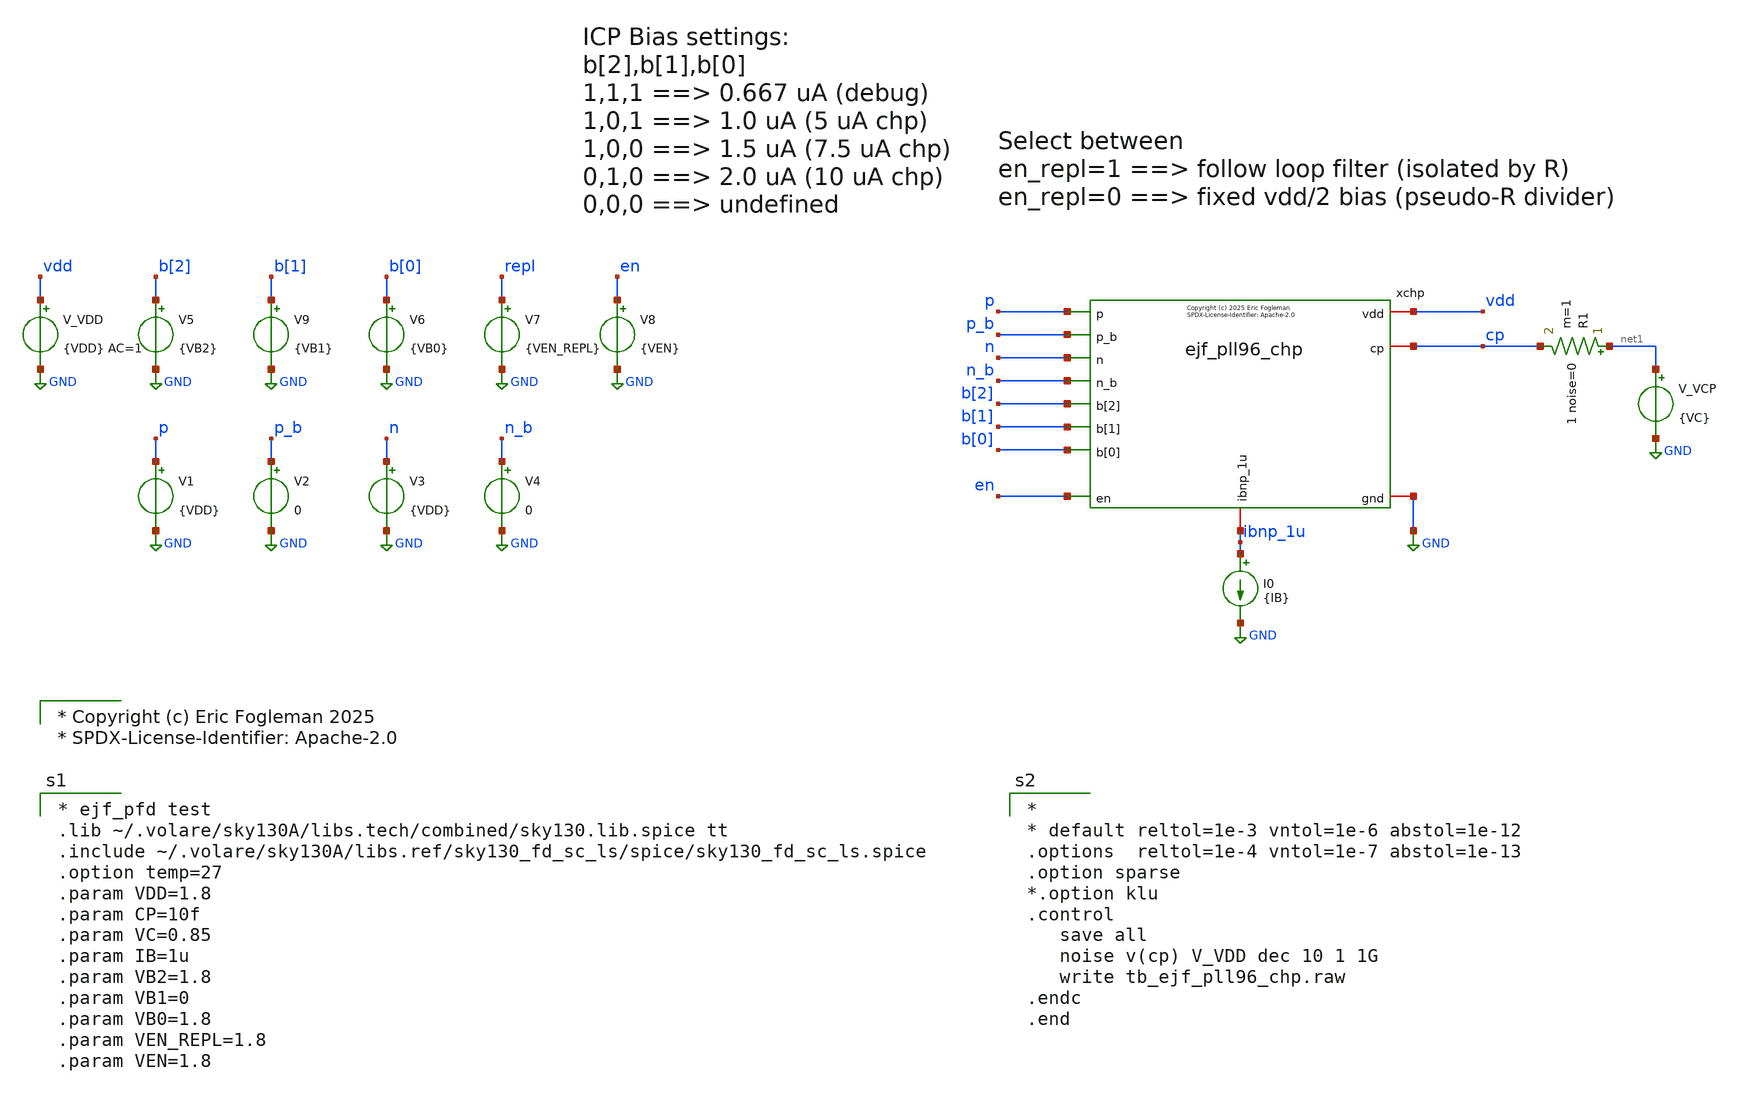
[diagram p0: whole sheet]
** sch_path: xschem/tb_ejf_pll96_chp.sch
* xschem/ejf_pll96_chp.sym:
* Copyright (c) 2025 Eric Fogleman

* Copyright (c) Eric Fogleman 2025
* SPDX-License-Identifier: Apache-2.0

**.subckt tb_ejf_pll96_chp
V_VDD vdd GND {VDD} AC=1
.save i(v_vdd)
xchp vdd p ibnp_1u p_b cp n_b n GND b[1] en b[2] b[0] ejf_pll96_chp
I0 ibnp_1u GND {IB}
V_VCP net1 GND {VC}
.save i(v_vcp)
V1 p GND {VDD}
.save i(v1)
V2 p_b GND 0
.save i(v2)
V3 n GND {VDD}
.save i(v3)
V4 n_b GND 0
.save i(v4)
R1 net1 cp 1 noise=0 m=1
V5 b[2] GND {VB2}
.save i(v5)
V6 b[0] GND {VB0}
.save i(v6)
V7 repl GND {VEN_REPL}
.save i(v7)
V8 en GND {VEN}
.save i(v8)
V9 b[1] GND {VB1}
.save i(v9)
**** begin user architecture code

* ejf_pfd test
.lib ~/.volare/sky130A/libs.tech/combined/sky130.lib.spice tt
.include ~/.volare/sky130A/libs.ref/sky130_fd_sc_ls/spice/sky130_fd_sc_ls.spice
.option temp=27
.param VDD=1.8
.param CP=10f
.param VC=0.85
.param IB=1u
.param VB2=1.8
.param VB1=0
.param VB0=1.8
.param VEN_REPL=1.8
.param VEN=1.8



*
* default reltol=1e-3 vntol=1e-6 abstol=1e-12
.options  reltol=1e-4 vntol=1e-7 abstol=1e-13
.option sparse
*.option klu
.control
   save all
   noise v(cp) V_VDD dec 10 1 1G
   write tb_ejf_pll96_chp.raw
.endc
.end

**** end user architecture code
**.ends

* expanding   symbol:  ejf_pll96_chp.sym # of pins=12
** sym_path: xschem/ejf_pll96_chp.sym
** sch_path: xschem/ejf_pll96_chp.sch
.subckt ejf_pll96_chp vdd p ibnp_1u p_b cp n_b n gnd b[1] en b[2] b[0]
*.iopin vdd
*.iopin gnd
*.iopin ibnp_1u
*.iopin cp
*.ipin p
*.ipin n_b
*.ipin p_b
*.ipin n
*.ipin en
*.ipin b[2]
*.ipin b[1]
*.ipin b[0]
XMP2_2[1] mp2d mp2_2g vdd vdd sky130_fd_pr__pfet_01v8_lvt L=1.2 W=0.6 nf=1 ad='int((nf+1)/2) * W/nf * 0.29'
+ as='int((nf+2)/2) * W/nf * 0.29' pd='2*int((nf+1)/2) * (W/nf + 0.29)' ps='2*int((nf+2)/2) * (W/nf + 0.29)'
+ nrd='0.29 / W' nrs='0.29 / W' sa=0 sb=0 sd=0 mult=1 m=1
XMP2_2[0] mp2d mp2_2g vdd vdd sky130_fd_pr__pfet_01v8_lvt L=1.2 W=0.6 nf=1 ad='int((nf+1)/2) * W/nf * 0.29'
+ as='int((nf+2)/2) * W/nf * 0.29' pd='2*int((nf+1)/2) * (W/nf + 0.29)' ps='2*int((nf+2)/2) * (W/nf + 0.29)'
+ nrd='0.29 / W' nrs='0.29 / W' sa=0 sb=0 sd=0 mult=1 m=1
XMN3 net1 mn1g gnd gnd sky130_fd_pr__nfet_01v8 L=1.2 W=0.6 nf=1 ad='int((nf+1)/2) * W/nf * 0.29' as='int((nf+2)/2) * W/nf * 0.29'
+ pd='2*int((nf+1)/2) * (W/nf + 0.29)' ps='2*int((nf+2)/2) * (W/nf + 0.29)' nrd='0.29 / W' nrs='0.29 / W'
+ sa=0 sb=0 sd=0 mult=1 m=1
XMN3C mn1g mn1cg net1 gnd sky130_fd_pr__nfet_01v8 L=0.3 W=0.6 nf=1 ad='int((nf+1)/2) * W/nf * 0.29' as='int((nf+2)/2) * W/nf * 0.29'
+ pd='2*int((nf+1)/2) * (W/nf + 0.29)' ps='2*int((nf+2)/2) * (W/nf + 0.29)' nrd='0.29 / W' nrs='0.29 / W'
+ sa=0 sb=0 sd=0 mult=1 m=1
XMP1[14] mp1d mp1g vdd vdd sky130_fd_pr__pfet_01v8_lvt L=1.2 W=0.6 nf=1 ad='int((nf+1)/2) * W/nf * 0.29'
+ as='int((nf+2)/2) * W/nf * 0.29' pd='2*int((nf+1)/2) * (W/nf + 0.29)' ps='2*int((nf+2)/2) * (W/nf + 0.29)'
+ nrd='0.29 / W' nrs='0.29 / W' sa=0 sb=0 sd=0 mult=1 m=1
XMP1[13] mp1d mp1g vdd vdd sky130_fd_pr__pfet_01v8_lvt L=1.2 W=0.6 nf=1 ad='int((nf+1)/2) * W/nf * 0.29'
+ as='int((nf+2)/2) * W/nf * 0.29' pd='2*int((nf+1)/2) * (W/nf + 0.29)' ps='2*int((nf+2)/2) * (W/nf + 0.29)'
+ nrd='0.29 / W' nrs='0.29 / W' sa=0 sb=0 sd=0 mult=1 m=1
XMP1[12] mp1d mp1g vdd vdd sky130_fd_pr__pfet_01v8_lvt L=1.2 W=0.6 nf=1 ad='int((nf+1)/2) * W/nf * 0.29'
+ as='int((nf+2)/2) * W/nf * 0.29' pd='2*int((nf+1)/2) * (W/nf + 0.29)' ps='2*int((nf+2)/2) * (W/nf + 0.29)'
+ nrd='0.29 / W' nrs='0.29 / W' sa=0 sb=0 sd=0 mult=1 m=1
XMP1[11] mp1d mp1g vdd vdd sky130_fd_pr__pfet_01v8_lvt L=1.2 W=0.6 nf=1 ad='int((nf+1)/2) * W/nf * 0.29'
+ as='int((nf+2)/2) * W/nf * 0.29' pd='2*int((nf+1)/2) * (W/nf + 0.29)' ps='2*int((nf+2)/2) * (W/nf + 0.29)'
+ nrd='0.29 / W' nrs='0.29 / W' sa=0 sb=0 sd=0 mult=1 m=1
XMP1[10] mp1d mp1g vdd vdd sky130_fd_pr__pfet_01v8_lvt L=1.2 W=0.6 nf=1 ad='int((nf+1)/2) * W/nf * 0.29'
+ as='int((nf+2)/2) * W/nf * 0.29' pd='2*int((nf+1)/2) * (W/nf + 0.29)' ps='2*int((nf+2)/2) * (W/nf + 0.29)'
+ nrd='0.29 / W' nrs='0.29 / W' sa=0 sb=0 sd=0 mult=1 m=1
XMP1[9] mp1d mp1g vdd vdd sky130_fd_pr__pfet_01v8_lvt L=1.2 W=0.6 nf=1 ad='int((nf+1)/2) * W/nf * 0.29'
+ as='int((nf+2)/2) * W/nf * 0.29' pd='2*int((nf+1)/2) * (W/nf + 0.29)' ps='2*int((nf+2)/2) * (W/nf + 0.29)'
+ nrd='0.29 / W' nrs='0.29 / W' sa=0 sb=0 sd=0 mult=1 m=1
XMP1[8] mp1d mp1g vdd vdd sky130_fd_pr__pfet_01v8_lvt L=1.2 W=0.6 nf=1 ad='int((nf+1)/2) * W/nf * 0.29'
+ as='int((nf+2)/2) * W/nf * 0.29' pd='2*int((nf+1)/2) * (W/nf + 0.29)' ps='2*int((nf+2)/2) * (W/nf + 0.29)'
+ nrd='0.29 / W' nrs='0.29 / W' sa=0 sb=0 sd=0 mult=1 m=1
XMP1[7] mp1d mp1g vdd vdd sky130_fd_pr__pfet_01v8_lvt L=1.2 W=0.6 nf=1 ad='int((nf+1)/2) * W/nf * 0.29'
+ as='int((nf+2)/2) * W/nf * 0.29' pd='2*int((nf+1)/2) * (W/nf + 0.29)' ps='2*int((nf+2)/2) * (W/nf + 0.29)'
+ nrd='0.29 / W' nrs='0.29 / W' sa=0 sb=0 sd=0 mult=1 m=1
XMP1[6] mp1d mp1g vdd vdd sky130_fd_pr__pfet_01v8_lvt L=1.2 W=0.6 nf=1 ad='int((nf+1)/2) * W/nf * 0.29'
+ as='int((nf+2)/2) * W/nf * 0.29' pd='2*int((nf+1)/2) * (W/nf + 0.29)' ps='2*int((nf+2)/2) * (W/nf + 0.29)'
+ nrd='0.29 / W' nrs='0.29 / W' sa=0 sb=0 sd=0 mult=1 m=1
XMP1[5] mp1d mp1g vdd vdd sky130_fd_pr__pfet_01v8_lvt L=1.2 W=0.6 nf=1 ad='int((nf+1)/2) * W/nf * 0.29'
+ as='int((nf+2)/2) * W/nf * 0.29' pd='2*int((nf+1)/2) * (W/nf + 0.29)' ps='2*int((nf+2)/2) * (W/nf + 0.29)'
+ nrd='0.29 / W' nrs='0.29 / W' sa=0 sb=0 sd=0 mult=1 m=1
XMP1[4] mp1d mp1g vdd vdd sky130_fd_pr__pfet_01v8_lvt L=1.2 W=0.6 nf=1 ad='int((nf+1)/2) * W/nf * 0.29'
+ as='int((nf+2)/2) * W/nf * 0.29' pd='2*int((nf+1)/2) * (W/nf + 0.29)' ps='2*int((nf+2)/2) * (W/nf + 0.29)'
+ nrd='0.29 / W' nrs='0.29 / W' sa=0 sb=0 sd=0 mult=1 m=1
XMP1[3] mp1d mp1g vdd vdd sky130_fd_pr__pfet_01v8_lvt L=1.2 W=0.6 nf=1 ad='int((nf+1)/2) * W/nf * 0.29'
+ as='int((nf+2)/2) * W/nf * 0.29' pd='2*int((nf+1)/2) * (W/nf + 0.29)' ps='2*int((nf+2)/2) * (W/nf + 0.29)'
+ nrd='0.29 / W' nrs='0.29 / W' sa=0 sb=0 sd=0 mult=1 m=1
XMP1[2] mp1d mp1g vdd vdd sky130_fd_pr__pfet_01v8_lvt L=1.2 W=0.6 nf=1 ad='int((nf+1)/2) * W/nf * 0.29'
+ as='int((nf+2)/2) * W/nf * 0.29' pd='2*int((nf+1)/2) * (W/nf + 0.29)' ps='2*int((nf+2)/2) * (W/nf + 0.29)'
+ nrd='0.29 / W' nrs='0.29 / W' sa=0 sb=0 sd=0 mult=1 m=1
XMP1[1] mp1d mp1g vdd vdd sky130_fd_pr__pfet_01v8_lvt L=1.2 W=0.6 nf=1 ad='int((nf+1)/2) * W/nf * 0.29'
+ as='int((nf+2)/2) * W/nf * 0.29' pd='2*int((nf+1)/2) * (W/nf + 0.29)' ps='2*int((nf+2)/2) * (W/nf + 0.29)'
+ nrd='0.29 / W' nrs='0.29 / W' sa=0 sb=0 sd=0 mult=1 m=1
XMP1[0] mp1d mp1g vdd vdd sky130_fd_pr__pfet_01v8_lvt L=1.2 W=0.6 nf=1 ad='int((nf+1)/2) * W/nf * 0.29'
+ as='int((nf+2)/2) * W/nf * 0.29' pd='2*int((nf+1)/2) * (W/nf + 0.29)' ps='2*int((nf+2)/2) * (W/nf + 0.29)'
+ nrd='0.29 / W' nrs='0.29 / W' sa=0 sb=0 sd=0 mult=1 m=1
XMP2C mp1g ibnp_1u mp2d vdd sky130_fd_pr__pfet_01v8_lvt L=0.35 W=1.2 nf=1 ad='int((nf+1)/2) * W/nf * 0.29'
+ as='int((nf+2)/2) * W/nf * 0.29' pd='2*int((nf+1)/2) * (W/nf + 0.29)' ps='2*int((nf+2)/2) * (W/nf + 0.29)'
+ nrd='0.29 / W' nrs='0.29 / W' sa=0 sb=0 sd=0 mult=1 m=1
XMP1C mp1cd ibnp_1u mp1d vdd sky130_fd_pr__pfet_01v8_lvt L=0.35 W=6 nf=5 ad='int((nf+1)/2) * W/nf * 0.29'
+ as='int((nf+2)/2) * W/nf * 0.29' pd='2*int((nf+1)/2) * (W/nf + 0.29)' ps='2*int((nf+2)/2) * (W/nf + 0.29)'
+ nrd='0.29 / W' nrs='0.29 / W' sa=0 sb=0 sd=0 mult=1 m=1
XMN1[4] mn1d mn1g gnd gnd sky130_fd_pr__nfet_01v8 L=1.2 W=0.6 nf=1 ad='int((nf+1)/2) * W/nf * 0.29' as='int((nf+2)/2) * W/nf * 0.29'
+ pd='2*int((nf+1)/2) * (W/nf + 0.29)' ps='2*int((nf+2)/2) * (W/nf + 0.29)' nrd='0.29 / W' nrs='0.29 / W'
+ sa=0 sb=0 sd=0 mult=1 m=1
XMN1[3] mn1d mn1g gnd gnd sky130_fd_pr__nfet_01v8 L=1.2 W=0.6 nf=1 ad='int((nf+1)/2) * W/nf * 0.29' as='int((nf+2)/2) * W/nf * 0.29'
+ pd='2*int((nf+1)/2) * (W/nf + 0.29)' ps='2*int((nf+2)/2) * (W/nf + 0.29)' nrd='0.29 / W' nrs='0.29 / W'
+ sa=0 sb=0 sd=0 mult=1 m=1
XMN1[2] mn1d mn1g gnd gnd sky130_fd_pr__nfet_01v8 L=1.2 W=0.6 nf=1 ad='int((nf+1)/2) * W/nf * 0.29' as='int((nf+2)/2) * W/nf * 0.29'
+ pd='2*int((nf+1)/2) * (W/nf + 0.29)' ps='2*int((nf+2)/2) * (W/nf + 0.29)' nrd='0.29 / W' nrs='0.29 / W'
+ sa=0 sb=0 sd=0 mult=1 m=1
XMN1[1] mn1d mn1g gnd gnd sky130_fd_pr__nfet_01v8 L=1.2 W=0.6 nf=1 ad='int((nf+1)/2) * W/nf * 0.29' as='int((nf+2)/2) * W/nf * 0.29'
+ pd='2*int((nf+1)/2) * (W/nf + 0.29)' ps='2*int((nf+2)/2) * (W/nf + 0.29)' nrd='0.29 / W' nrs='0.29 / W'
+ sa=0 sb=0 sd=0 mult=1 m=1
XMN1[0] mn1d mn1g gnd gnd sky130_fd_pr__nfet_01v8 L=1.2 W=0.6 nf=1 ad='int((nf+1)/2) * W/nf * 0.29' as='int((nf+2)/2) * W/nf * 0.29'
+ pd='2*int((nf+1)/2) * (W/nf + 0.29)' ps='2*int((nf+2)/2) * (W/nf + 0.29)' nrd='0.29 / W' nrs='0.29 / W'
+ sa=0 sb=0 sd=0 mult=1 m=1
XM1C mn1cd mn1cg mn1d gnd sky130_fd_pr__nfet_01v8 L=0.3 W=3.0 nf=5 ad='int((nf+1)/2) * W/nf * 0.29' as='int((nf+2)/2) * W/nf * 0.29'
+ pd='2*int((nf+1)/2) * (W/nf + 0.29)' ps='2*int((nf+2)/2) * (W/nf + 0.29)' nrd='0.29 / W' nrs='0.29 / W'
+ sa=0 sb=0 sd=0 mult=1 m=1
XMP11 cp_repl p mp1cd vdd sky130_fd_pr__pfet_01v8 L=0.15 W=1 nf=1 ad='int((nf+1)/2) * W/nf * 0.29' as='int((nf+2)/2) * W/nf * 0.29'
+ pd='2*int((nf+1)/2) * (W/nf + 0.29)' ps='2*int((nf+2)/2) * (W/nf + 0.29)' nrd='0.29 / W' nrs='0.29 / W'
+ sa=0 sb=0 sd=0 mult=1 m=1
XMN11 cp_repl n_b mn1cd gnd sky130_fd_pr__nfet_01v8 L=0.15 W=1 nf=1 ad='int((nf+1)/2) * W/nf * 0.29'
+ as='int((nf+2)/2) * W/nf * 0.29' pd='2*int((nf+1)/2) * (W/nf + 0.29)' ps='2*int((nf+2)/2) * (W/nf + 0.29)'
+ nrd='0.29 / W' nrs='0.29 / W' sa=0 sb=0 sd=0 mult=1 m=1
XMP10 cp p_b mp1cd vdd sky130_fd_pr__pfet_01v8 L=0.15 W=1 nf=1 ad='int((nf+1)/2) * W/nf * 0.29' as='int((nf+2)/2) * W/nf * 0.29'
+ pd='2*int((nf+1)/2) * (W/nf + 0.29)' ps='2*int((nf+2)/2) * (W/nf + 0.29)' nrd='0.29 / W' nrs='0.29 / W'
+ sa=0 sb=0 sd=0 mult=1 m=1
XMN10 cp n mn1cd gnd sky130_fd_pr__nfet_01v8 L=0.15 W=1 nf=1 ad='int((nf+1)/2) * W/nf * 0.29' as='int((nf+2)/2) * W/nf * 0.29'
+ pd='2*int((nf+1)/2) * (W/nf + 0.29)' ps='2*int((nf+2)/2) * (W/nf + 0.29)' nrd='0.29 / W' nrs='0.29 / W'
+ sa=0 sb=0 sd=0 mult=1 m=1
XMP20[5] mp20d mp1g vdd vdd sky130_fd_pr__pfet_01v8_lvt L=1.2 W=0.6 nf=1 ad='int((nf+1)/2) * W/nf * 0.29'
+ as='int((nf+2)/2) * W/nf * 0.29' pd='2*int((nf+1)/2) * (W/nf + 0.29)' ps='2*int((nf+2)/2) * (W/nf + 0.29)'
+ nrd='0.29 / W' nrs='0.29 / W' sa=0 sb=0 sd=0 mult=1 m=1
XMP20[4] mp20d mp1g vdd vdd sky130_fd_pr__pfet_01v8_lvt L=1.2 W=0.6 nf=1 ad='int((nf+1)/2) * W/nf * 0.29'
+ as='int((nf+2)/2) * W/nf * 0.29' pd='2*int((nf+1)/2) * (W/nf + 0.29)' ps='2*int((nf+2)/2) * (W/nf + 0.29)'
+ nrd='0.29 / W' nrs='0.29 / W' sa=0 sb=0 sd=0 mult=1 m=1
XMP20[3] mp20d mp1g vdd vdd sky130_fd_pr__pfet_01v8_lvt L=1.2 W=0.6 nf=1 ad='int((nf+1)/2) * W/nf * 0.29'
+ as='int((nf+2)/2) * W/nf * 0.29' pd='2*int((nf+1)/2) * (W/nf + 0.29)' ps='2*int((nf+2)/2) * (W/nf + 0.29)'
+ nrd='0.29 / W' nrs='0.29 / W' sa=0 sb=0 sd=0 mult=1 m=1
XMP20[2] mp20d mp1g vdd vdd sky130_fd_pr__pfet_01v8_lvt L=1.2 W=0.6 nf=1 ad='int((nf+1)/2) * W/nf * 0.29'
+ as='int((nf+2)/2) * W/nf * 0.29' pd='2*int((nf+1)/2) * (W/nf + 0.29)' ps='2*int((nf+2)/2) * (W/nf + 0.29)'
+ nrd='0.29 / W' nrs='0.29 / W' sa=0 sb=0 sd=0 mult=1 m=1
XMP20[1] mp20d mp1g vdd vdd sky130_fd_pr__pfet_01v8_lvt L=1.2 W=0.6 nf=1 ad='int((nf+1)/2) * W/nf * 0.29'
+ as='int((nf+2)/2) * W/nf * 0.29' pd='2*int((nf+1)/2) * (W/nf + 0.29)' ps='2*int((nf+2)/2) * (W/nf + 0.29)'
+ nrd='0.29 / W' nrs='0.29 / W' sa=0 sb=0 sd=0 mult=1 m=1
XMP20[0] mp20d mp1g vdd vdd sky130_fd_pr__pfet_01v8_lvt L=1.2 W=0.6 nf=1 ad='int((nf+1)/2) * W/nf * 0.29'
+ as='int((nf+2)/2) * W/nf * 0.29' pd='2*int((nf+1)/2) * (W/nf + 0.29)' ps='2*int((nf+2)/2) * (W/nf + 0.29)'
+ nrd='0.29 / W' nrs='0.29 / W' sa=0 sb=0 sd=0 mult=1 m=1
XMN30 mn1cg en_b gnd gnd sky130_fd_pr__nfet_01v8 L=0.15 W=0.6 nf=1 ad='int((nf+1)/2) * W/nf * 0.29' as='int((nf+2)/2) * W/nf * 0.29'
+ pd='2*int((nf+1)/2) * (W/nf + 0.29)' ps='2*int((nf+2)/2) * (W/nf + 0.29)' nrd='0.29 / W' nrs='0.29 / W'
+ sa=0 sb=0 sd=0 mult=1 m=1
XMN31 mn1g en_b gnd gnd sky130_fd_pr__nfet_01v8 L=0.15 W=0.6 nf=1 ad='int((nf+1)/2) * W/nf * 0.29' as='int((nf+2)/2) * W/nf * 0.29'
+ pd='2*int((nf+1)/2) * (W/nf + 0.29)' ps='2*int((nf+2)/2) * (W/nf + 0.29)' nrd='0.29 / W' nrs='0.29 / W'
+ sa=0 sb=0 sd=0 mult=1 m=1
XMP21P mn25g amp_inp mp20d vdd sky130_fd_pr__pfet_01v8_lvt L=0.35 W=0.6 nf=1 ad='int((nf+1)/2) * W/nf * 0.29'
+ as='int((nf+2)/2) * W/nf * 0.29' pd='2*int((nf+1)/2) * (W/nf + 0.29)' ps='2*int((nf+2)/2) * (W/nf + 0.29)'
+ nrd='0.29 / W' nrs='0.29 / W' sa=0 sb=0 sd=0 mult=1 m=1
XMP21N net3 cp_repl mp20d vdd sky130_fd_pr__pfet_01v8_lvt L=0.35 W=0.6 nf=1 ad='int((nf+1)/2) * W/nf * 0.29'
+ as='int((nf+2)/2) * W/nf * 0.29' pd='2*int((nf+1)/2) * (W/nf + 0.29)' ps='2*int((nf+2)/2) * (W/nf + 0.29)'
+ nrd='0.29 / W' nrs='0.29 / W' sa=0 sb=0 sd=0 mult=1 m=1
XMN24 net2 net3 gnd gnd sky130_fd_pr__nfet_01v8 L=1.2 W=0.6 nf=1 ad='int((nf+1)/2) * W/nf * 0.29' as='int((nf+2)/2) * W/nf * 0.29'
+ pd='2*int((nf+1)/2) * (W/nf + 0.29)' ps='2*int((nf+2)/2) * (W/nf + 0.29)' nrd='0.29 / W' nrs='0.29 / W'
+ sa=0 sb=0 sd=0 mult=1 m=1
XMN23 net17 net3 gnd gnd sky130_fd_pr__nfet_01v8 L=1.2 W=0.6 nf=1 ad='int((nf+1)/2) * W/nf * 0.29' as='int((nf+2)/2) * W/nf * 0.29'
+ pd='2*int((nf+1)/2) * (W/nf + 0.29)' ps='2*int((nf+2)/2) * (W/nf + 0.29)' nrd='0.29 / W' nrs='0.29 / W'
+ sa=0 sb=0 sd=0 mult=1 m=1
XMN24C net3 mn1cg net2 gnd sky130_fd_pr__nfet_01v8 L=0.3 W=0.6 nf=1 ad='int((nf+1)/2) * W/nf * 0.29'
+ as='int((nf+2)/2) * W/nf * 0.29' pd='2*int((nf+1)/2) * (W/nf + 0.29)' ps='2*int((nf+2)/2) * (W/nf + 0.29)'
+ nrd='0.29 / W' nrs='0.29 / W' sa=0 sb=0 sd=0 mult=1 m=1
XMN23C mn25g mn1cg net17 gnd sky130_fd_pr__nfet_01v8 L=0.3 W=0.6 nf=1 ad='int((nf+1)/2) * W/nf * 0.29'
+ as='int((nf+2)/2) * W/nf * 0.29' pd='2*int((nf+1)/2) * (W/nf + 0.29)' ps='2*int((nf+2)/2) * (W/nf + 0.29)'
+ nrd='0.29 / W' nrs='0.29 / W' sa=0 sb=0 sd=0 mult=1 m=1
XMP2_1 mp2d mp2_1g vdd vdd sky130_fd_pr__pfet_01v8_lvt L=1.2 W=0.6 nf=1 ad='int((nf+1)/2) * W/nf * 0.29'
+ as='int((nf+2)/2) * W/nf * 0.29' pd='2*int((nf+1)/2) * (W/nf + 0.29)' ps='2*int((nf+2)/2) * (W/nf + 0.29)'
+ nrd='0.29 / W' nrs='0.29 / W' sa=0 sb=0 sd=0 mult=1 m=1
XMP2_1P5 mp2d mp2_1p5g vdd vdd sky130_fd_pr__pfet_01v8_lvt L=1.2 W=0.9 nf=1 ad='int((nf+1)/2) * W/nf * 0.29'
+ as='int((nf+2)/2) * W/nf * 0.29' pd='2*int((nf+1)/2) * (W/nf + 0.29)' ps='2*int((nf+2)/2) * (W/nf + 0.29)'
+ nrd='0.29 / W' nrs='0.29 / W' sa=0 sb=0 sd=0 mult=1 m=1
XMP32 mp2_1p5g b_bb[1] vdd vdd sky130_fd_pr__pfet_01v8_hvt L=0.15 W=1.2 nf=1 ad='int((nf+1)/2) * W/nf * 0.29'
+ as='int((nf+2)/2) * W/nf * 0.29' pd='2*int((nf+1)/2) * (W/nf + 0.29)' ps='2*int((nf+2)/2) * (W/nf + 0.29)'
+ nrd='0.29 / W' nrs='0.29 / W' sa=0 sb=0 sd=0 mult=1 m=1
XMP3C mn1g ibnp_1u net4 vdd sky130_fd_pr__pfet_01v8_lvt L=0.35 W=1.2 nf=1 ad='int((nf+1)/2) * W/nf * 0.29'
+ as='int((nf+2)/2) * W/nf * 0.29' pd='2*int((nf+1)/2) * (W/nf + 0.29)' ps='2*int((nf+2)/2) * (W/nf + 0.29)'
+ nrd='0.29 / W' nrs='0.29 / W' sa=0 sb=0 sd=0 mult=1 m=1
XMP3[2] net4 mp1g vdd vdd sky130_fd_pr__pfet_01v8_lvt L=1.2 W=0.6 nf=mult=1 ad='int((nf+1)/2) * W/nf * 0.29'
+ as='int((nf+2)/2) * W/nf * 0.29' pd='2*int((nf+1)/2) * (W/nf + 0.29)' ps='2*int((nf+2)/2) * (W/nf + 0.29)'
+ nrd='0.29 / W' nrs='0.29 / W' sa=0 sb=0 sd=0 mult=1 m=1
XMP3[1] net4 mp1g vdd vdd sky130_fd_pr__pfet_01v8_lvt L=1.2 W=0.6 nf=mult=1 ad='int((nf+1)/2) * W/nf * 0.29'
+ as='int((nf+2)/2) * W/nf * 0.29' pd='2*int((nf+1)/2) * (W/nf + 0.29)' ps='2*int((nf+2)/2) * (W/nf + 0.29)'
+ nrd='0.29 / W' nrs='0.29 / W' sa=0 sb=0 sd=0 mult=1 m=1
XMP3[0] net4 mp1g vdd vdd sky130_fd_pr__pfet_01v8_lvt L=1.2 W=0.6 nf=mult=1 ad='int((nf+1)/2) * W/nf * 0.29'
+ as='int((nf+2)/2) * W/nf * 0.29' pd='2*int((nf+1)/2) * (W/nf + 0.29)' ps='2*int((nf+2)/2) * (W/nf + 0.29)'
+ nrd='0.29 / W' nrs='0.29 / W' sa=0 sb=0 sd=0 mult=1 m=1
x1 vdd en en_bb en_b gnd ejf_pll96_dbuf
x3[2] vdd b[2] b_bb[2] b_b[2] gnd ejf_pll96_dbuf
x3[1] vdd b[1] b_bb[1] b_b[1] gnd ejf_pll96_dbuf
x3[0] vdd b[0] b_bb[0] b_b[0] gnd ejf_pll96_dbuf
XMP42 mp1g b_b[1] mp2_1p5g vdd sky130_fd_pr__pfet_01v8_hvt L=0.15 W=1.2 nf=1 ad='int((nf+1)/2) * W/nf * 0.29'
+ as='int((nf+2)/2) * W/nf * 0.29' pd='2*int((nf+1)/2) * (W/nf + 0.29)' ps='2*int((nf+2)/2) * (W/nf + 0.29)'
+ nrd='0.29 / W' nrs='0.29 / W' sa=0 sb=0 sd=0 mult=1 m=1
XMP33 mp2_1g b_bb[0] vdd vdd sky130_fd_pr__pfet_01v8_hvt L=0.15 W=1.2 nf=1 ad='int((nf+1)/2) * W/nf * 0.29'
+ as='int((nf+2)/2) * W/nf * 0.29' pd='2*int((nf+1)/2) * (W/nf + 0.29)' ps='2*int((nf+2)/2) * (W/nf + 0.29)'
+ nrd='0.29 / W' nrs='0.29 / W' sa=0 sb=0 sd=0 mult=1 m=1
XMP43 mp1g b_b[0] mp2_1g vdd sky130_fd_pr__pfet_01v8_hvt L=0.15 W=1.2 nf=1 ad='int((nf+1)/2) * W/nf * 0.29'
+ as='int((nf+2)/2) * W/nf * 0.29' pd='2*int((nf+1)/2) * (W/nf + 0.29)' ps='2*int((nf+2)/2) * (W/nf + 0.29)'
+ nrd='0.29 / W' nrs='0.29 / W' sa=0 sb=0 sd=0 mult=1 m=1
XMP30 ibnp_1u en_bb vdd vdd sky130_fd_pr__pfet_01v8_hvt L=0.15 W=0.6 nf=1 ad='int((nf+1)/2) * W/nf * 0.29'
+ as='int((nf+2)/2) * W/nf * 0.29' pd='2*int((nf+1)/2) * (W/nf + 0.29)' ps='2*int((nf+2)/2) * (W/nf + 0.29)'
+ nrd='0.29 / W' nrs='0.29 / W' sa=0 sb=0 sd=0 mult=1 m=1
XMP31 mp1g en_bb vdd vdd sky130_fd_pr__pfet_01v8_hvt L=0.15 W=0.6 nf=1 ad='int((nf+1)/2) * W/nf * 0.29'
+ as='int((nf+2)/2) * W/nf * 0.29' pd='2*int((nf+1)/2) * (W/nf + 0.29)' ps='2*int((nf+2)/2) * (W/nf + 0.29)'
+ nrd='0.29 / W' nrs='0.29 / W' sa=0 sb=0 sd=0 mult=1 m=1
XR5[1] vdd vdd vdd sky130_fd_pr__res_xhigh_po_0p69 L=8.97 mult=1 m=1
XR5[0] vdd vdd vdd sky130_fd_pr__res_xhigh_po_0p69 L=8.97 mult=1 m=1
XMP34 mp2_2g b_bb[2] vdd vdd sky130_fd_pr__pfet_01v8_hvt L=0.15 W=1.2 nf=1 ad='int((nf+1)/2) * W/nf * 0.29'
+ as='int((nf+2)/2) * W/nf * 0.29' pd='2*int((nf+1)/2) * (W/nf + 0.29)' ps='2*int((nf+2)/2) * (W/nf + 0.29)'
+ nrd='0.29 / W' nrs='0.29 / W' sa=0 sb=0 sd=0 mult=1 m=1
XMP44 mp1g b_b[2] mp2_2g vdd sky130_fd_pr__pfet_01v8_hvt L=0.15 W=1.2 nf=1 ad='int((nf+1)/2) * W/nf * 0.29'
+ as='int((nf+2)/2) * W/nf * 0.29' pd='2*int((nf+1)/2) * (W/nf + 0.29)' ps='2*int((nf+2)/2) * (W/nf + 0.29)'
+ nrd='0.29 / W' nrs='0.29 / W' sa=0 sb=0 sd=0 mult=1 m=1
**** begin user architecture code

* Copyright (c) Eric Fogleman 2025
* SPDX-License-Identifier: Apache-2.0

**** end user architecture code
XR1 net6 net7 vdd sky130_fd_pr__res_xhigh_po_0p69 L=8.97 mult=1 m=1
XR2 ibnp_1u net6 vdd sky130_fd_pr__res_xhigh_po_0p69 L=8.97 mult=1 m=1
XR3 net7 net5 vdd sky130_fd_pr__res_xhigh_po_0p69 L=8.97 mult=1 m=1
XR4 net5 mp1g vdd sky130_fd_pr__res_xhigh_po_0p69 L=8.97 mult=1 m=1
XMP4C mn1cg ibnp_1u net9 vdd sky130_fd_pr__pfet_01v8_lvt L=0.35 W=1.2 nf=1 ad='int((nf+1)/2) * W/nf * 0.29'
+ as='int((nf+2)/2) * W/nf * 0.29' pd='2*int((nf+1)/2) * (W/nf + 0.29)' ps='2*int((nf+2)/2) * (W/nf + 0.29)'
+ nrd='0.29 / W' nrs='0.29 / W' sa=0 sb=0 sd=0 mult=1 m=1
XMP4[2] net9 mp1g vdd vdd sky130_fd_pr__pfet_01v8_lvt L=1.2 W=0.6 nf=mult=1 ad='int((nf+1)/2) * W/nf * 0.29'
+ as='int((nf+2)/2) * W/nf * 0.29' pd='2*int((nf+1)/2) * (W/nf + 0.29)' ps='2*int((nf+2)/2) * (W/nf + 0.29)'
+ nrd='0.29 / W' nrs='0.29 / W' sa=0 sb=0 sd=0 mult=1 m=1
XMP4[1] net9 mp1g vdd vdd sky130_fd_pr__pfet_01v8_lvt L=1.2 W=0.6 nf=mult=1 ad='int((nf+1)/2) * W/nf * 0.29'
+ as='int((nf+2)/2) * W/nf * 0.29' pd='2*int((nf+1)/2) * (W/nf + 0.29)' ps='2*int((nf+2)/2) * (W/nf + 0.29)'
+ nrd='0.29 / W' nrs='0.29 / W' sa=0 sb=0 sd=0 mult=1 m=1
XMP4[0] net9 mp1g vdd vdd sky130_fd_pr__pfet_01v8_lvt L=1.2 W=0.6 nf=mult=1 ad='int((nf+1)/2) * W/nf * 0.29'
+ as='int((nf+2)/2) * W/nf * 0.29' pd='2*int((nf+1)/2) * (W/nf + 0.29)' ps='2*int((nf+2)/2) * (W/nf + 0.29)'
+ nrd='0.29 / W' nrs='0.29 / W' sa=0 sb=0 sd=0 mult=1 m=1
XMN4[0] net12 mn1cg gnd gnd sky130_fd_pr__nfet_01v8 L=1.2 W=0.6 nf=1 ad='int((nf+1)/2) * W/nf * 0.29'
+ as='int((nf+2)/2) * W/nf * 0.29' pd='2*int((nf+1)/2) * (W/nf + 0.29)' ps='2*int((nf+2)/2) * (W/nf + 0.29)'
+ nrd='0.29 / W' nrs='0.29 / W' sa=0 sb=0 sd=0 mult=1 m=1
XMN4[1] net11 mn1cg net12 gnd sky130_fd_pr__nfet_01v8 L=1.2 W=0.6 nf=1 ad='int((nf+1)/2) * W/nf * 0.29'
+ as='int((nf+2)/2) * W/nf * 0.29' pd='2*int((nf+1)/2) * (W/nf + 0.29)' ps='2*int((nf+2)/2) * (W/nf + 0.29)'
+ nrd='0.29 / W' nrs='0.29 / W' sa=0 sb=0 sd=0 mult=1 m=1
XMN4[2] net10 mn1cg net11 gnd sky130_fd_pr__nfet_01v8 L=1.2 W=0.6 nf=1 ad='int((nf+1)/2) * W/nf * 0.29'
+ as='int((nf+2)/2) * W/nf * 0.29' pd='2*int((nf+1)/2) * (W/nf + 0.29)' ps='2*int((nf+2)/2) * (W/nf + 0.29)'
+ nrd='0.29 / W' nrs='0.29 / W' sa=0 sb=0 sd=0 mult=1 m=1
XMN4[3] net13 mn1cg net10 gnd sky130_fd_pr__nfet_01v8 L=1.2 W=0.6 nf=1 ad='int((nf+1)/2) * W/nf * 0.29'
+ as='int((nf+2)/2) * W/nf * 0.29' pd='2*int((nf+1)/2) * (W/nf + 0.29)' ps='2*int((nf+2)/2) * (W/nf + 0.29)'
+ nrd='0.29 / W' nrs='0.29 / W' sa=0 sb=0 sd=0 mult=1 m=1
XMN4[4] net15 mn1cg net13 gnd sky130_fd_pr__nfet_01v8 L=1.2 W=0.6 nf=1 ad='int((nf+1)/2) * W/nf * 0.29'
+ as='int((nf+2)/2) * W/nf * 0.29' pd='2*int((nf+1)/2) * (W/nf + 0.29)' ps='2*int((nf+2)/2) * (W/nf + 0.29)'
+ nrd='0.29 / W' nrs='0.29 / W' sa=0 sb=0 sd=0 mult=1 m=1
XR14 cp net8 vdd sky130_fd_pr__res_xhigh_po_0p69 L=8.97 mult=1 m=1
XR13 net8 amp_inp vdd sky130_fd_pr__res_xhigh_po_0p69 L=8.97 mult=1 m=1
XMP2 mp1d mp1g vdd vdd sky130_fd_pr__pfet_01v8_lvt L=1.2 W=0.6 nf=1 ad='int((nf+1)/2) * W/nf * 0.29'
+ as='int((nf+2)/2) * W/nf * 0.29' pd='2*int((nf+1)/2) * (W/nf + 0.29)' ps='2*int((nf+2)/2) * (W/nf + 0.29)'
+ nrd='0.29 / W' nrs='0.29 / W' sa=0 sb=0 sd=0 mult=6 m=6
XMP1 cp_repl ibnp_1u mp1d vdd sky130_fd_pr__pfet_01v8_lvt L=0.35 W=2.4 nf=2 ad='int((nf+1)/2) * W/nf * 0.29'
+ as='int((nf+2)/2) * W/nf * 0.29' pd='2*int((nf+1)/2) * (W/nf + 0.29)' ps='2*int((nf+2)/2) * (W/nf + 0.29)'
+ nrd='0.29 / W' nrs='0.29 / W' sa=0 sb=0 sd=0 mult=1 m=1
XMN25 net14 mn25g gnd gnd sky130_fd_pr__nfet_01v8 L=1.2 W=1.2 nf=2 ad='int((nf+1)/2) * W/nf * 0.29' as='int((nf+2)/2) * W/nf * 0.29'
+ pd='2*int((nf+1)/2) * (W/nf + 0.29)' ps='2*int((nf+2)/2) * (W/nf + 0.29)' nrd='0.29 / W' nrs='0.29 / W'
+ sa=0 sb=0 sd=0 mult=1 m=1
XMN25C cp_repl mn1cg net14 gnd sky130_fd_pr__nfet_01v8 L=0.3 W=1.2 nf=2 ad='int((nf+1)/2) * W/nf * 0.29'
+ as='int((nf+2)/2) * W/nf * 0.29' pd='2*int((nf+1)/2) * (W/nf + 0.29)' ps='2*int((nf+2)/2) * (W/nf + 0.29)'
+ nrd='0.29 / W' nrs='0.29 / W' sa=0 sb=0 sd=0 mult=1 m=1
XC1 net18 cp_repl sky130_fd_pr__cap_mim_m3_1 W=12 L=12 MF=1 m=1
XMN4[5] mn1cg mn1cg net15 gnd sky130_fd_pr__nfet_01v8 L=1.2 W=0.6 nf=1 ad='int((nf+1)/2) * W/nf * 0.29'
+ as='int((nf+2)/2) * W/nf * 0.29' pd='2*int((nf+1)/2) * (W/nf + 0.29)' ps='2*int((nf+2)/2) * (W/nf + 0.29)'
+ nrd='0.29 / W' nrs='0.29 / W' sa=0 sb=0 sd=0 mult=1 m=1
XR5 net16 mn25g gnd sky130_fd_pr__res_xhigh_po_0p69 L=7.59 mult=1 m=1
XR6 net18 net16 gnd sky130_fd_pr__res_xhigh_po_0p69 L=7.59 mult=1 m=1
XMNCAP1 gnd cp_repl gnd gnd sky130_fd_pr__nfet_01v8 L=2 W=8 nf=2 ad='int((nf+1)/2) * W/nf * 0.29' as='int((nf+2)/2) * W/nf * 0.29'
+ pd='2*int((nf+1)/2) * (W/nf + 0.29)' ps='2*int((nf+2)/2) * (W/nf + 0.29)' nrd='0.29 / W' nrs='0.29 / W'
+ sa=0 sb=0 sd=0 mult=1 m=1
XMNCAP2 gnd mn1cg gnd gnd sky130_fd_pr__nfet_01v8 L=2 W=8 nf=2 ad='int((nf+1)/2) * W/nf * 0.29' as='int((nf+2)/2) * W/nf * 0.29'
+ pd='2*int((nf+1)/2) * (W/nf + 0.29)' ps='2*int((nf+2)/2) * (W/nf + 0.29)' nrd='0.29 / W' nrs='0.29 / W'
+ sa=0 sb=0 sd=0 mult=1 m=1
.ends


* expanding   symbol:  ejf_pll96_dbuf.sym # of pins=5
** sym_path: xschem/ejf_pll96_dbuf.sym
** sch_path: xschem/ejf_pll96_dbuf.sch
.subckt ejf_pll96_dbuf vdd a y y_b gnd
*.ipin a
*.iopin vdd
*.iopin gnd
*.opin y
*.opin y_b
XMP1 y_b a vdd vdd sky130_fd_pr__pfet_01v8_hvt L=0.15 W=1.2 nf=1 ad='int((nf+1)/2) * W/nf * 0.29' as='int((nf+2)/2) * W/nf * 0.29'
+ pd='2*int((nf+1)/2) * (W/nf + 0.29)' ps='2*int((nf+2)/2) * (W/nf + 0.29)' nrd='0.29 / W' nrs='0.29 / W'
+ sa=0 sb=0 sd=0 mult=1 m=1
XMP3 y y_b vdd vdd sky130_fd_pr__pfet_01v8_hvt L=0.15 W=1.2 nf=1 ad='int((nf+1)/2) * W/nf * 0.29' as='int((nf+2)/2) * W/nf * 0.29'
+ pd='2*int((nf+1)/2) * (W/nf + 0.29)' ps='2*int((nf+2)/2) * (W/nf + 0.29)' nrd='0.29 / W' nrs='0.29 / W'
+ sa=0 sb=0 sd=0 mult=1 m=1
XMN4 y y_b gnd gnd sky130_fd_pr__nfet_01v8 L=0.15 W=0.74 nf=1 ad='int((nf+1)/2) * W/nf * 0.29' as='int((nf+2)/2) * W/nf * 0.29'
+ pd='2*int((nf+1)/2) * (W/nf + 0.29)' ps='2*int((nf+2)/2) * (W/nf + 0.29)' nrd='0.29 / W' nrs='0.29 / W'
+ sa=0 sb=0 sd=0 mult=1 m=1
XMN2 y_b a gnd gnd sky130_fd_pr__nfet_01v8 L=0.15 W=0.74 nf=1 ad='int((nf+1)/2) * W/nf * 0.29' as='int((nf+2)/2) * W/nf * 0.29'
+ pd='2*int((nf+1)/2) * (W/nf + 0.29)' ps='2*int((nf+2)/2) * (W/nf + 0.29)' nrd='0.29 / W' nrs='0.29 / W'
+ sa=0 sb=0 sd=0 mult=1 m=1
**** begin user architecture code

* Copyright (c) Eric Fogleman 2025
* SPDX-License-Identifier: Apache-2.0

**** end user architecture code
.ends

.GLOBAL GND
.end
